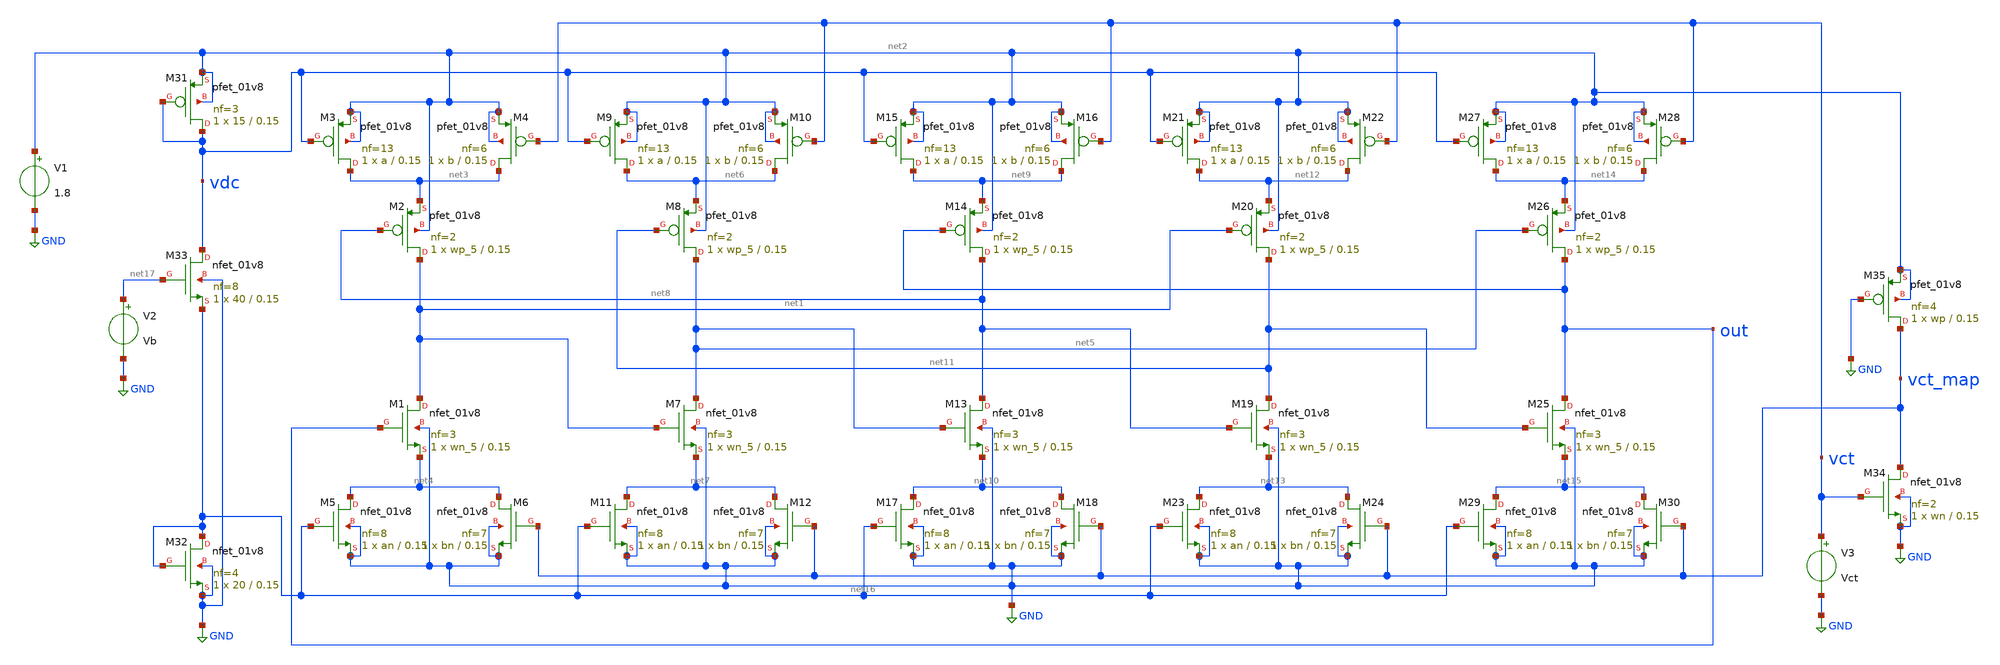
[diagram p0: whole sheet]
** sch_path: 5_Stage_VCRO_CSA.sch
**.subckt 5_Stage_VCRO_CSA
XM1 net1 out net4 GND sky130_fd_pr__nfet_01v8 L=0.15 W=wn_5 nf=3 ad='int((nf+1)/2) * W/nf * 0.29' as='int((nf+2)/2) * W/nf * 0.29'
+ pd='2*int((nf+1)/2) * (W/nf + 0.29)' ps='2*int((nf+2)/2) * (W/nf + 0.29)' nrd='0.29 / W' nrs='0.29 / W'
+ sa=0 sb=0 sd=0 mult=1 m=1
XM2 net1 net8 net3 net2 sky130_fd_pr__pfet_01v8 L=0.15 W=wp_5 nf=2 ad='int((nf+1)/2) * W/nf * 0.29' as='int((nf+2)/2) * W/nf * 0.29'
+ pd='2*int((nf+1)/2) * (W/nf + 0.29)' ps='2*int((nf+2)/2) * (W/nf + 0.29)' nrd='0.29 / W' nrs='0.29 / W'
+ sa=0 sb=0 sd=0 mult=1 m=1
XM3 net3 vdc net2 net2 sky130_fd_pr__pfet_01v8 L=0.15 W=a nf=13 ad='int((nf+1)/2) * W/nf * 0.29' as='int((nf+2)/2) * W/nf * 0.29'
+ pd='2*int((nf+1)/2) * (W/nf + 0.29)' ps='2*int((nf+2)/2) * (W/nf + 0.29)' nrd='0.29 / W' nrs='0.29 / W'
+ sa=0 sb=0 sd=0 mult=1 m=1
XM4 net3 vct net2 net2 sky130_fd_pr__pfet_01v8 L=0.15 W=b nf=6 ad='int((nf+1)/2) * W/nf * 0.29' as='int((nf+2)/2) * W/nf * 0.29'
+ pd='2*int((nf+1)/2) * (W/nf + 0.29)' ps='2*int((nf+2)/2) * (W/nf + 0.29)' nrd='0.29 / W' nrs='0.29 / W'
+ sa=0 sb=0 sd=0 mult=1 m=1
XM5 net4 net16 GND GND sky130_fd_pr__nfet_01v8 L=0.15 W=an nf=8 ad='int((nf+1)/2) * W/nf * 0.29' as='int((nf+2)/2) * W/nf * 0.29'
+ pd='2*int((nf+1)/2) * (W/nf + 0.29)' ps='2*int((nf+2)/2) * (W/nf + 0.29)' nrd='0.29 / W' nrs='0.29 / W'
+ sa=0 sb=0 sd=0 mult=1 m=1
XM6 net4 vct_map GND GND sky130_fd_pr__nfet_01v8 L=0.15 W=bn nf=7 ad='int((nf+1)/2) * W/nf * 0.29' as='int((nf+2)/2) * W/nf * 0.29'
+ pd='2*int((nf+1)/2) * (W/nf + 0.29)' ps='2*int((nf+2)/2) * (W/nf + 0.29)' nrd='0.29 / W' nrs='0.29 / W'
+ sa=0 sb=0 sd=0 mult=1 m=1
XM7 net5 net1 net7 GND sky130_fd_pr__nfet_01v8 L=0.15 W=wn_5 nf=3 ad='int((nf+1)/2) * W/nf * 0.29' as='int((nf+2)/2) * W/nf * 0.29'
+ pd='2*int((nf+1)/2) * (W/nf + 0.29)' ps='2*int((nf+2)/2) * (W/nf + 0.29)' nrd='0.29 / W' nrs='0.29 / W'
+ sa=0 sb=0 sd=0 mult=1 m=1
XM8 net5 net11 net6 net2 sky130_fd_pr__pfet_01v8 L=0.15 W=wp_5 nf=2 ad='int((nf+1)/2) * W/nf * 0.29'
+ as='int((nf+2)/2) * W/nf * 0.29' pd='2*int((nf+1)/2) * (W/nf + 0.29)' ps='2*int((nf+2)/2) * (W/nf + 0.29)'
+ nrd='0.29 / W' nrs='0.29 / W' sa=0 sb=0 sd=0 mult=1 m=1
XM9 net6 vdc net2 net2 sky130_fd_pr__pfet_01v8 L=0.15 W=a nf=13 ad='int((nf+1)/2) * W/nf * 0.29' as='int((nf+2)/2) * W/nf * 0.29'
+ pd='2*int((nf+1)/2) * (W/nf + 0.29)' ps='2*int((nf+2)/2) * (W/nf + 0.29)' nrd='0.29 / W' nrs='0.29 / W'
+ sa=0 sb=0 sd=0 mult=1 m=1
XM10 net6 vct net2 net2 sky130_fd_pr__pfet_01v8 L=0.15 W=b nf=6 ad='int((nf+1)/2) * W/nf * 0.29' as='int((nf+2)/2) * W/nf * 0.29'
+ pd='2*int((nf+1)/2) * (W/nf + 0.29)' ps='2*int((nf+2)/2) * (W/nf + 0.29)' nrd='0.29 / W' nrs='0.29 / W'
+ sa=0 sb=0 sd=0 mult=1 m=1
XM11 net7 net16 GND GND sky130_fd_pr__nfet_01v8 L=0.15 W=an nf=8 ad='int((nf+1)/2) * W/nf * 0.29' as='int((nf+2)/2) * W/nf * 0.29'
+ pd='2*int((nf+1)/2) * (W/nf + 0.29)' ps='2*int((nf+2)/2) * (W/nf + 0.29)' nrd='0.29 / W' nrs='0.29 / W'
+ sa=0 sb=0 sd=0 mult=1 m=1
XM12 net7 vct_map GND GND sky130_fd_pr__nfet_01v8 L=0.15 W=bn nf=7 ad='int((nf+1)/2) * W/nf * 0.29' as='int((nf+2)/2) * W/nf * 0.29'
+ pd='2*int((nf+1)/2) * (W/nf + 0.29)' ps='2*int((nf+2)/2) * (W/nf + 0.29)' nrd='0.29 / W' nrs='0.29 / W'
+ sa=0 sb=0 sd=0 mult=1 m=1
XM13 net8 net5 net10 GND sky130_fd_pr__nfet_01v8 L=0.15 W=wn_5 nf=3 ad='int((nf+1)/2) * W/nf * 0.29'
+ as='int((nf+2)/2) * W/nf * 0.29' pd='2*int((nf+1)/2) * (W/nf + 0.29)' ps='2*int((nf+2)/2) * (W/nf + 0.29)'
+ nrd='0.29 / W' nrs='0.29 / W' sa=0 sb=0 sd=0 mult=1 m=1
XM14 net8 out net9 net2 sky130_fd_pr__pfet_01v8 L=0.15 W=wp_5 nf=2 ad='int((nf+1)/2) * W/nf * 0.29' as='int((nf+2)/2) * W/nf * 0.29'
+ pd='2*int((nf+1)/2) * (W/nf + 0.29)' ps='2*int((nf+2)/2) * (W/nf + 0.29)' nrd='0.29 / W' nrs='0.29 / W'
+ sa=0 sb=0 sd=0 mult=1 m=1
XM15 net9 vdc net2 net2 sky130_fd_pr__pfet_01v8 L=0.15 W=a nf=13 ad='int((nf+1)/2) * W/nf * 0.29' as='int((nf+2)/2) * W/nf * 0.29'
+ pd='2*int((nf+1)/2) * (W/nf + 0.29)' ps='2*int((nf+2)/2) * (W/nf + 0.29)' nrd='0.29 / W' nrs='0.29 / W'
+ sa=0 sb=0 sd=0 mult=1 m=1
XM16 net9 vct net2 net2 sky130_fd_pr__pfet_01v8 L=0.15 W=b nf=6 ad='int((nf+1)/2) * W/nf * 0.29' as='int((nf+2)/2) * W/nf * 0.29'
+ pd='2*int((nf+1)/2) * (W/nf + 0.29)' ps='2*int((nf+2)/2) * (W/nf + 0.29)' nrd='0.29 / W' nrs='0.29 / W'
+ sa=0 sb=0 sd=0 mult=1 m=1
XM17 net10 net16 GND GND sky130_fd_pr__nfet_01v8 L=0.15 W=an nf=8 ad='int((nf+1)/2) * W/nf * 0.29' as='int((nf+2)/2) * W/nf * 0.29'
+ pd='2*int((nf+1)/2) * (W/nf + 0.29)' ps='2*int((nf+2)/2) * (W/nf + 0.29)' nrd='0.29 / W' nrs='0.29 / W'
+ sa=0 sb=0 sd=0 mult=1 m=1
XM18 net10 vct_map GND GND sky130_fd_pr__nfet_01v8 L=0.15 W=bn nf=7 ad='int((nf+1)/2) * W/nf * 0.29'
+ as='int((nf+2)/2) * W/nf * 0.29' pd='2*int((nf+1)/2) * (W/nf + 0.29)' ps='2*int((nf+2)/2) * (W/nf + 0.29)'
+ nrd='0.29 / W' nrs='0.29 / W' sa=0 sb=0 sd=0 mult=1 m=1
XM19 net11 net8 net13 GND sky130_fd_pr__nfet_01v8 L=0.15 W=wn_5 nf=3 ad='int((nf+1)/2) * W/nf * 0.29'
+ as='int((nf+2)/2) * W/nf * 0.29' pd='2*int((nf+1)/2) * (W/nf + 0.29)' ps='2*int((nf+2)/2) * (W/nf + 0.29)'
+ nrd='0.29 / W' nrs='0.29 / W' sa=0 sb=0 sd=0 mult=1 m=1
XM20 net11 net1 net12 net2 sky130_fd_pr__pfet_01v8 L=0.15 W=wp_5 nf=2 ad='int((nf+1)/2) * W/nf * 0.29'
+ as='int((nf+2)/2) * W/nf * 0.29' pd='2*int((nf+1)/2) * (W/nf + 0.29)' ps='2*int((nf+2)/2) * (W/nf + 0.29)'
+ nrd='0.29 / W' nrs='0.29 / W' sa=0 sb=0 sd=0 mult=1 m=1
XM21 net12 vdc net2 net2 sky130_fd_pr__pfet_01v8 L=0.15 W=a nf=13 ad='int((nf+1)/2) * W/nf * 0.29' as='int((nf+2)/2) * W/nf * 0.29'
+ pd='2*int((nf+1)/2) * (W/nf + 0.29)' ps='2*int((nf+2)/2) * (W/nf + 0.29)' nrd='0.29 / W' nrs='0.29 / W'
+ sa=0 sb=0 sd=0 mult=1 m=1
XM22 net12 vct net2 net2 sky130_fd_pr__pfet_01v8 L=0.15 W=b nf=6 ad='int((nf+1)/2) * W/nf * 0.29' as='int((nf+2)/2) * W/nf * 0.29'
+ pd='2*int((nf+1)/2) * (W/nf + 0.29)' ps='2*int((nf+2)/2) * (W/nf + 0.29)' nrd='0.29 / W' nrs='0.29 / W'
+ sa=0 sb=0 sd=0 mult=1 m=1
XM23 net13 net16 GND GND sky130_fd_pr__nfet_01v8 L=0.15 W=an nf=8 ad='int((nf+1)/2) * W/nf * 0.29' as='int((nf+2)/2) * W/nf * 0.29'
+ pd='2*int((nf+1)/2) * (W/nf + 0.29)' ps='2*int((nf+2)/2) * (W/nf + 0.29)' nrd='0.29 / W' nrs='0.29 / W'
+ sa=0 sb=0 sd=0 mult=1 m=1
XM24 net13 vct_map GND GND sky130_fd_pr__nfet_01v8 L=0.15 W=bn nf=7 ad='int((nf+1)/2) * W/nf * 0.29'
+ as='int((nf+2)/2) * W/nf * 0.29' pd='2*int((nf+1)/2) * (W/nf + 0.29)' ps='2*int((nf+2)/2) * (W/nf + 0.29)'
+ nrd='0.29 / W' nrs='0.29 / W' sa=0 sb=0 sd=0 mult=1 m=1
XM25 out net11 net15 GND sky130_fd_pr__nfet_01v8 L=0.15 W=wn_5 nf=3 ad='int((nf+1)/2) * W/nf * 0.29'
+ as='int((nf+2)/2) * W/nf * 0.29' pd='2*int((nf+1)/2) * (W/nf + 0.29)' ps='2*int((nf+2)/2) * (W/nf + 0.29)'
+ nrd='0.29 / W' nrs='0.29 / W' sa=0 sb=0 sd=0 mult=1 m=1
XM26 out net5 net14 net2 sky130_fd_pr__pfet_01v8 L=0.15 W=wp_5 nf=2 ad='int((nf+1)/2) * W/nf * 0.29'
+ as='int((nf+2)/2) * W/nf * 0.29' pd='2*int((nf+1)/2) * (W/nf + 0.29)' ps='2*int((nf+2)/2) * (W/nf + 0.29)'
+ nrd='0.29 / W' nrs='0.29 / W' sa=0 sb=0 sd=0 mult=1 m=1
XM27 net14 vdc net2 net2 sky130_fd_pr__pfet_01v8 L=0.15 W=a nf=13 ad='int((nf+1)/2) * W/nf * 0.29' as='int((nf+2)/2) * W/nf * 0.29'
+ pd='2*int((nf+1)/2) * (W/nf + 0.29)' ps='2*int((nf+2)/2) * (W/nf + 0.29)' nrd='0.29 / W' nrs='0.29 / W'
+ sa=0 sb=0 sd=0 mult=1 m=1
XM28 net14 vct net2 net2 sky130_fd_pr__pfet_01v8 L=0.15 W=b nf=6 ad='int((nf+1)/2) * W/nf * 0.29' as='int((nf+2)/2) * W/nf * 0.29'
+ pd='2*int((nf+1)/2) * (W/nf + 0.29)' ps='2*int((nf+2)/2) * (W/nf + 0.29)' nrd='0.29 / W' nrs='0.29 / W'
+ sa=0 sb=0 sd=0 mult=1 m=1
XM29 net15 net16 GND GND sky130_fd_pr__nfet_01v8 L=0.15 W=an nf=8 ad='int((nf+1)/2) * W/nf * 0.29' as='int((nf+2)/2) * W/nf * 0.29'
+ pd='2*int((nf+1)/2) * (W/nf + 0.29)' ps='2*int((nf+2)/2) * (W/nf + 0.29)' nrd='0.29 / W' nrs='0.29 / W'
+ sa=0 sb=0 sd=0 mult=1 m=1
XM30 net15 vct_map GND GND sky130_fd_pr__nfet_01v8 L=0.15 W=bn nf=7 ad='int((nf+1)/2) * W/nf * 0.29'
+ as='int((nf+2)/2) * W/nf * 0.29' pd='2*int((nf+1)/2) * (W/nf + 0.29)' ps='2*int((nf+2)/2) * (W/nf + 0.29)'
+ nrd='0.29 / W' nrs='0.29 / W' sa=0 sb=0 sd=0 mult=1 m=1
V1 net2 GND 1.8
XM31 vdc vdc net2 net2 sky130_fd_pr__pfet_01v8 L=0.15 W=15 nf=3 ad='int((nf+1)/2) * W/nf * 0.29' as='int((nf+2)/2) * W/nf * 0.29'
+ pd='2*int((nf+1)/2) * (W/nf + 0.29)' ps='2*int((nf+2)/2) * (W/nf + 0.29)' nrd='0.29 / W' nrs='0.29 / W'
+ sa=0 sb=0 sd=0 mult=1 m=1
XM32 net16 net16 GND GND sky130_fd_pr__nfet_01v8 L=0.15 W=20 nf=4 ad='int((nf+1)/2) * W/nf * 0.29' as='int((nf+2)/2) * W/nf * 0.29'
+ pd='2*int((nf+1)/2) * (W/nf + 0.29)' ps='2*int((nf+2)/2) * (W/nf + 0.29)' nrd='0.29 / W' nrs='0.29 / W'
+ sa=0 sb=0 sd=0 mult=1 m=1
XM34 vct_map vct GND GND sky130_fd_pr__nfet_01v8 L=0.15 W=wn nf=2 ad='int((nf+1)/2) * W/nf * 0.29' as='int((nf+2)/2) * W/nf * 0.29'
+ pd='2*int((nf+1)/2) * (W/nf + 0.29)' ps='2*int((nf+2)/2) * (W/nf + 0.29)' nrd='0.29 / W' nrs='0.29 / W'
+ sa=0 sb=0 sd=0 mult=1 m=1
V3 vct GND Vct
XM35 vct_map GND net2 net2 sky130_fd_pr__pfet_01v8 L=0.15 W=wp nf=4 ad='int((nf+1)/2) * W/nf * 0.29'
+ as='int((nf+2)/2) * W/nf * 0.29' pd='2*int((nf+1)/2) * (W/nf + 0.29)' ps='2*int((nf+2)/2) * (W/nf + 0.29)'
+ nrd='0.29 / W' nrs='0.29 / W' sa=0 sb=0 sd=0 mult=1 m=1
XM33 vdc net17 net16 GND sky130_fd_pr__nfet_01v8 L=0.15 W=40 nf=8 ad='int((nf+1)/2) * W/nf * 0.29' as='int((nf+2)/2) * W/nf * 0.29'
+ pd='2*int((nf+1)/2) * (W/nf + 0.29)' ps='2*int((nf+2)/2) * (W/nf + 0.29)' nrd='0.29 / W' nrs='0.29 / W'
+ sa=0 sb=0 sd=0 mult=1 m=1
V2 net17 GND Vb
**** begin user architecture code
 .include /home/foundry/skywater_pdk/skywater-pdk/libraries/sky130_fd_pr_ngspice/latest/models/corners/tt/nonfet.spice
.include /home/foundry/skywater_pdk/skywater-pdk/libraries/sky130_fd_pr_ngspice/latest/models/all.spice
.include /home/foundry/skywater_pdk/skywater-pdk/libraries/sky130_fd_pr/latest/cells/pfet_01v8_lvt/sky130_fd_pr__pfet_01v8_lvt__tt.corner.spice
.include /home/foundry/skywater_pdk/skywater-pdk/libraries/sky130_fd_pr/latest/cells/nfet_01v8_lvt/sky130_fd_pr__nfet_01v8_lvt__tt.corner.spice
.include /home/foundry/skywater_pdk/skywater-pdk/libraries/sky130_fd_pr/latest/cells/pfet_01v8_lvt/sky130_fd_pr__pfet_01v8_lvt__mismatch.corner.spice
.include /home/foundry/skywater_pdk/skywater-pdk/libraries/sky130_fd_pr/latest/cells/nfet_01v8_lvt/sky130_fd_pr__nfet_01v8_lvt__mismatch.corner.spice
.include /home/foundry/skywater_pdk/skywater-pdk/libraries/sky130_fd_pr/latest/cells/pfet_01v8/sky130_fd_pr__pfet_01v8__tt.corner.spice
.include /home/foundry/skywater_pdk/skywater-pdk/libraries/sky130_fd_pr/latest/cells/nfet_01v8/sky130_fd_pr__nfet_01v8__tt.corner.spice
.include /home/foundry/skywater_pdk/skywater-pdk/libraries/sky130_fd_pr/latest/cells/pfet_01v8/sky130_fd_pr__pfet_01v8__mismatch.corner.spice
.include /home/foundry/skywater_pdk/skywater-pdk/libraries/sky130_fd_pr/latest/cells/nfet_01v8/sky130_fd_pr__nfet_01v8__mismatch.corner.spice
.param mc_mm_switch=0
.param mc_pr_switch=0


.param a=65 b=30
.param an=40 bn=35
.param wn=6 wp=20
.param Vb=1.8 Vct=1.1
.param wn_5=15 wp_5=10
.IC v(out)=1.8
.func frequency(t) {1/t}
.control
      let v_start=0
      let v_end=1.8
      let v_step=0.2
      let length=(v_end/v_step)+1
      let v_temp=v_start
      let freq=unitvec(length)
      let v_control=unitvec(length)
      let v_map=unitvec(length)
      let count=0
      while v_temp le v_end
            alter V3 v_temp
            let v_control[count]=v_temp
            tran 1000p 20n UIC
	    meas tran yeval FIND v(vct_map) AT=10n
	    let v_map[count]=yeval
            meas tran tdiff TRIG v(out) VAL=0.9 RISE=65 TARG v(out) VAL=0.9 RISE=66
            let freq[count]=frequency(tdiff)
            let v_temp=v_temp+v_step
            let count=count+1
            echo after while loop %loop
      end
      write 5_Stage_VCRO_CSA.raw
      plot freq vs v_control
      plot v_map vs v_control
.endc
.save all

**** end user architecture code
**.ends
.GLOBAL GND
.end
